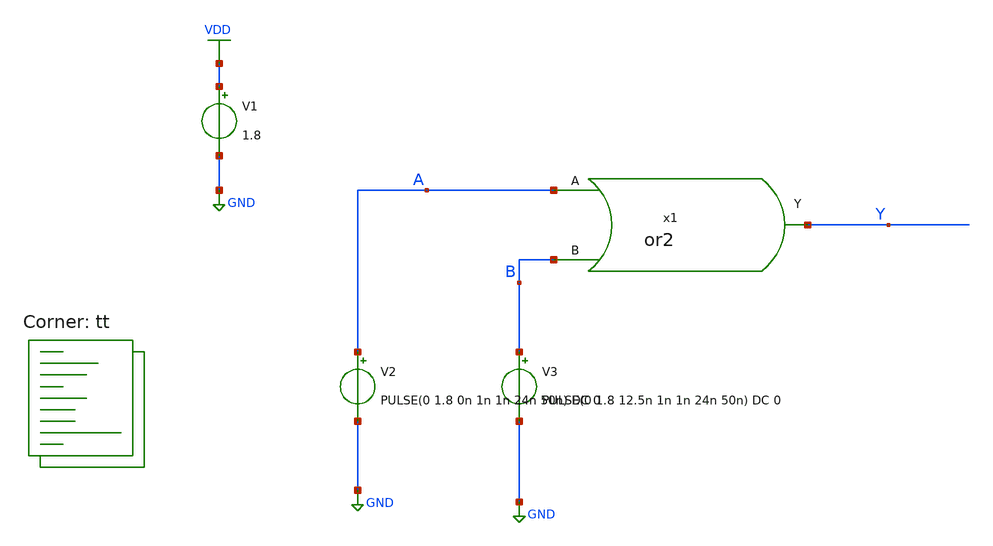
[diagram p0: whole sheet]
** sch_path: eng331lab_final/eng331lab_xschem/tb_or2.sch
**.subckt tb_or2
x1 A Y B or2
V1 VDD GND 1.8
V2 A GND PULSE(0 1.8 0n 1n 1n 24n 50n) DC 0
V3 B GND PULSE(0 1.8 12.5n 1n 1n 24n 50n) DC 0
**** begin user architecture code

.control
  save all
  tran 10n 400n
  write tb_or2.raw
  appendwrite
.endc


.lib $::SKYWATER_MODELS/sky130.lib.spice tt
**** end user architecture code
**.ends

* expanding   symbol:  eng331lab_xschem/or2.sym # of pins=3
** sym_path: eng331lab_final/eng331lab_xschem/or2.sym
** sch_path: eng331lab_final/eng331lab_xschem/or2.sch
.subckt or2 A Y B
*.ipin A
*.ipin B
*.opin Y
x1 A B Y_bar nor2
x2 Y Y_bar inv
.ends


* expanding   symbol:  eng331_debug/eng331lab_xschem/nor2.sym # of pins=3
** sym_path: eng331lab_final/eng331lab_xschem/nor2.sym
** sch_path: eng331lab_final/eng331lab_xschem/nor2.sch
.subckt nor2 A B Y
*.ipin A
*.ipin B
*.opin Y
XM1 net1 A VDD VDD sky130_fd_pr__pfet_01v8 L=0.15 W=1.6 nf=1 ad='int((1 + 1)/2) * 1.6 / 1 * 0.29' as='int((1 + 2)/2) * 1.6 / 1 * 0.29'
+ pd='2*int((1 + 1)/2) * (1.6 / 1 + 0.29)' ps='2*int((1 + 2)/2) * (1.6 / 1 + 0.29)' nrd='0.29 / 1.6 ' nrs='0.29 / 1.6 '
+ sa=0 sb=0 sd=0 mult=1 m=1
XM2 Y B net1 VDD sky130_fd_pr__pfet_01v8 L=0.15 W=1.6 nf=1 ad='int((1 + 1)/2) * 1.6 / 1 * 0.29' as='int((1 + 2)/2) * 1.6 / 1 * 0.29'
+ pd='2*int((1 + 1)/2) * (1.6 / 1 + 0.29)' ps='2*int((1 + 2)/2) * (1.6 / 1 + 0.29)' nrd='0.29 / 1.6 ' nrs='0.29 / 1.6 '
+ sa=0 sb=0 sd=0 mult=1 m=1
XM3 Y A GND GND sky130_fd_pr__nfet_01v8 L=0.15 W=0.5 nf=1 ad='int((1 + 1)/2) * 0.5 / 1 * 0.29' as='int((1 + 2)/2) * 0.5 / 1 * 0.29'
+ pd='2*int((1 + 1)/2) * (0.5 / 1 + 0.29)' ps='2*int((1 + 2)/2) * (0.5 / 1 + 0.29)' nrd='0.29 / 0.5 ' nrs='0.29 / 0.5 '
+ sa=0 sb=0 sd=0 mult=1 m=1
XM4 Y B GND GND sky130_fd_pr__nfet_01v8 L=0.15 W=0.5 nf=1 ad='int((1 + 1)/2) * 0.5 / 1 * 0.29' as='int((1 + 2)/2) * 0.5 / 1 * 0.29'
+ pd='2*int((1 + 1)/2) * (0.5 / 1 + 0.29)' ps='2*int((1 + 2)/2) * (0.5 / 1 + 0.29)' nrd='0.29 / 0.5 ' nrs='0.29 / 0.5 '
+ sa=0 sb=0 sd=0 mult=1 m=1
.ends


* expanding   symbol:  eng331_debug/eng331lab_xschem/inv.sym # of pins=2
** sym_path: eng331lab_final/eng331lab_xschem/inv.sym
** sch_path: eng331lab_final/eng331lab_xschem/inv.sch
.subckt inv Y A
*.ipin A
*.opin Y
XM1 Y A VDD VDD sky130_fd_pr__pfet_01v8 L=0.15 W=0.8 nf=1 ad='int((1 + 1)/2) * 0.8 / 1 * 0.29' as='int((1 + 2)/2) * 0.8 / 1 * 0.29'
+ pd='2*int((1 + 1)/2) * (0.8 / 1 + 0.29)' ps='2*int((1 + 2)/2) * (0.8 / 1 + 0.29)' nrd='0.29 / 0.8 ' nrs='0.29 / 0.8 '
+ sa=0 sb=0 sd=0 mult=1 m=1
XM2 Y A GND GND sky130_fd_pr__nfet_01v8 L=0.15 W=0.5 nf=1 ad='int((1 + 1)/2) * 0.5 / 1 * 0.29' as='int((1 + 2)/2) * 0.5 / 1 * 0.29'
+ pd='2*int((1 + 1)/2) * (0.5 / 1 + 0.29)' ps='2*int((1 + 2)/2) * (0.5 / 1 + 0.29)' nrd='0.29 / 0.5 ' nrs='0.29 / 0.5 '
+ sa=0 sb=0 sd=0 mult=1 m=1
.ends

.GLOBAL VDD
.GLOBAL GND
.end
